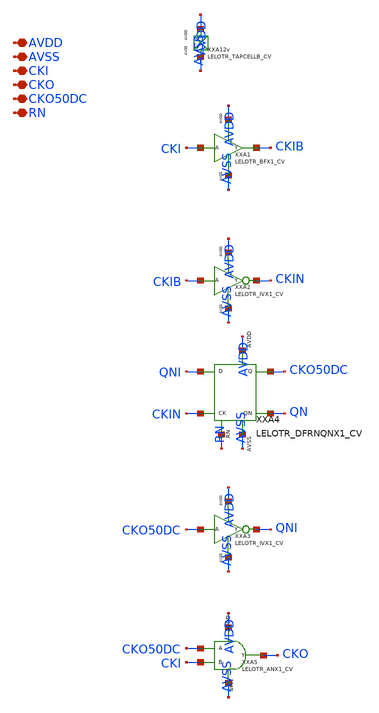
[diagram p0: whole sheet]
** sch_path: design/LELO_TR_GF180MCUD/LELOTR_CKDIV2_CV.sch
**.subckt LELOTR_CKDIV2_CV AVDD AVSS CKI CKO CKO50DC RN
*.iopin AVDD
*.iopin AVSS
*.iopin CKI
*.iopin CKO
*.iopin CKO50DC
*.iopin RN
XXA12v AVDD AVSS LELOTR_TAPCELLB_CV xoffset=0 yoffset=0 angle=0
XXA1 CKI CKIB AVDD AVSS LELOTR_BFX1_CV
XXA2 CKIB CKIN AVDD AVSS LELOTR_IVX1_CV
XXA4 QNI CKIN RN CKO50DC QN AVDD AVSS LELOTR_DFRNQNX1_CV
XXA3 CKO50DC QNI AVDD AVSS LELOTR_IVX1_CV
XXA5 CKO50DC CKI CKO AVDD AVSS LELOTR_ANX1_CV
**.ends
.end
